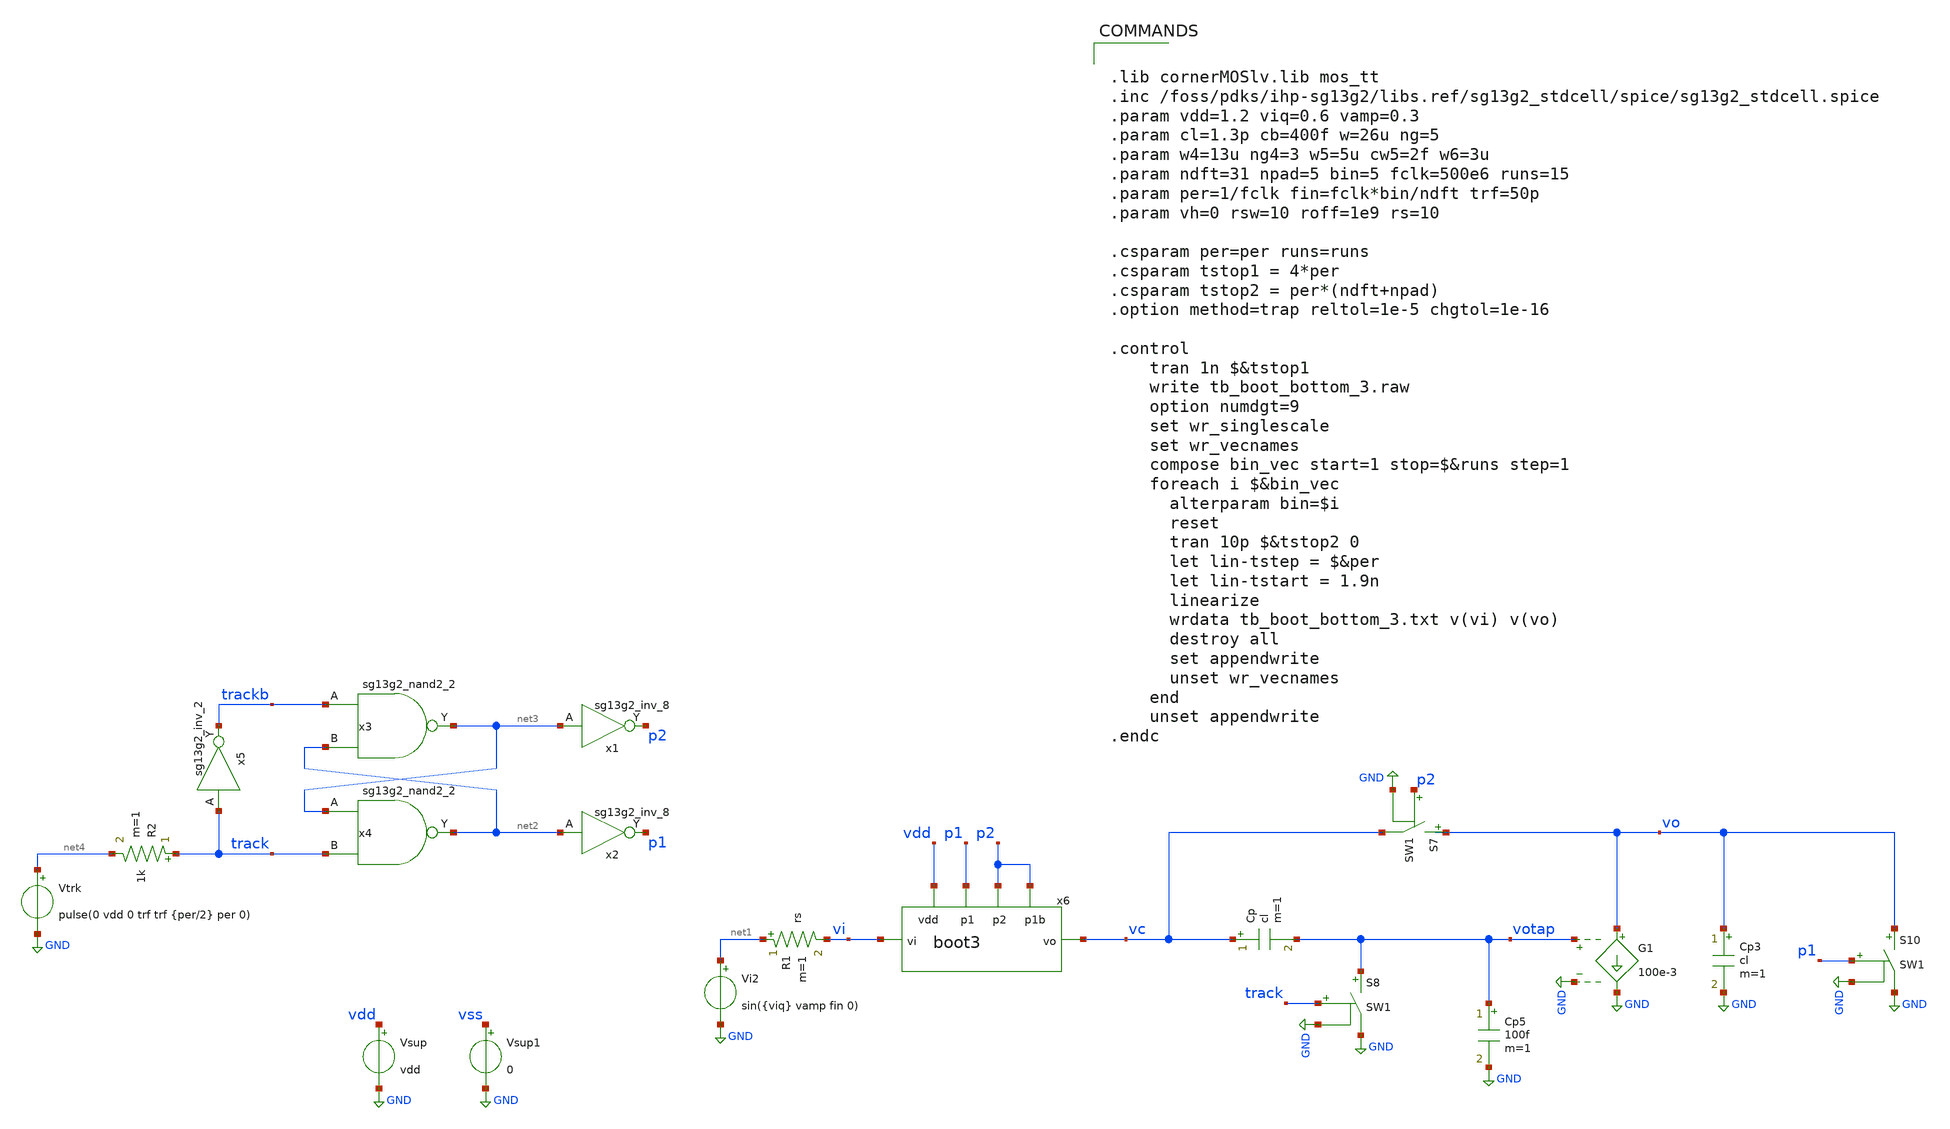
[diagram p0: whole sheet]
** sch_path: xschem/tb_boot_bottom_3.sch
* IHP-GmbH/IHP-Open-PDK/ihp-sg13g2/libs.tech/xschem/sg13g2_stdcells/sg13g2_inv_2.sch:
* Copyright 2023 IHP PDK Authors
* Licensed under the Apache License, Version 2.0 (the "License");
**.subckt tb_boot_bottom_3
Vi2 net1 GND sin({viq} vamp fin 0)
x1 p2 net3 VDD VSS sg13g2_inv_8
x2 p1 net2 VDD VSS sg13g2_inv_8
x3 net3 trackb net2 VDD VSS sg13g2_nand2_2
x4 net2 net3 track VDD VSS sg13g2_nand2_2
x5 trackb track VDD VSS sg13g2_inv_2
Vtrk net4 GND pulse(0 vdd 0 trf trf {per/2} per 0)
Vsup vdd GND vdd
Vsup1 vss GND 0
R1 net1 vi rs m=1
Cp vc votap cl m=1
G1 vo GND votap GND 100e-3
S7 vo vc p2 GND SW1
Cp3 vo GND cl m=1
S8 votap GND track GND SW1
S10 vo GND p1 GND SW1
Cp5 votap GND 100f m=1
x6 vdd p1 p2 vc vi p2 boot3
R2 track net4 1k m=1
**** begin user architecture code


.lib cornerMOSlv.lib mos_tt
.inc /foss/pdks/ihp-sg13g2/libs.ref/sg13g2_stdcell/spice/sg13g2_stdcell.spice
.param vdd=1.2 viq=0.6 vamp=0.3
.param cl=1.3p cb=400f w=26u ng=5
.param w4=13u ng4=3 w5=5u cw5=2f w6=3u
.param ndft=31 npad=5 bin=5 fclk=500e6 runs=15
.param per=1/fclk fin=fclk*bin/ndft trf=50p
.param vh=0 rsw=10 roff=1e9 rs=10

.csparam per=per runs=runs
.csparam tstop1 = 4*per
.csparam tstop2 = per*(ndft+npad)
.option method=trap reltol=1e-5 chgtol=1e-16

.control
    tran 1n $&tstop1
    write tb_boot_bottom_3.raw
    option numdgt=9
    set wr_singlescale
    set wr_vecnames
    compose bin_vec start=1 stop=$&runs step=1
    foreach i $&bin_vec
      alterparam bin=$i
      reset
      tran 10p $&tstop2 0
      let lin-tstep = $&per
      let lin-tstart = 1.9n
      linearize
      wrdata tb_boot_bottom_3.txt v(vi) v(vo)
      destroy all
      set appendwrite
      unset wr_vecnames
    end
    unset appendwrite
.endc


**** end user architecture code
**.ends

* expanding   symbol:  sg13g2_stdcells/sg13g2_inv_8.sym # of pins=2
** sym_path: sg13g2_stdcells/sg13g2_inv_8.sym
** sch_path: sg13g2_stdcells/sg13g2_inv_8.sch
.subckt sg13g2_inv_8 Y A VDD VSS
*.opin Y
*.ipin A
*.iopin VDD
*.iopin VSS
XM1 Y A VSS VSS sg13_lv_nmos w=5.92u l=130.00n ng=8 m=1 mm_ok=1
XM2 Y A VDD VDD sg13_lv_pmos w=8.96u l=130.00n ng=8 m=1 mm_ok=1
.ends


* expanding   symbol:  sg13g2_stdcells/sg13g2_nand2_2.sym # of pins=3
** sym_path: sg13g2_stdcells/sg13g2_nand2_2.sym
** sch_path: sg13g2_stdcells/sg13g2_nand2_2.sch
.subckt sg13g2_nand2_2 Y A B VDD VSS
*.iopin VDD
*.iopin VSS
*.opin Y
*.ipin B
*.ipin A
XM1 Y A net1 VSS sg13_lv_nmos w=1.44u l=130.00n ng=2 m=1 mm_ok=1
XM2 net1 B VSS VSS sg13_lv_nmos w=1.44u l=130.00n ng=2 m=1 mm_ok=1
XM3 Y A VDD VDD sg13_lv_pmos w=2.24u l=130.00n ng=2 m=1 mm_ok=1
XM4 Y B VDD VDD sg13_lv_pmos w=2.24u l=130.00n ng=2 m=1 mm_ok=1
.ends


* expanding   symbol:  sg13g2_stdcells/sg13g2_inv_2.sym # of pins=2
** sym_path: sg13g2_stdcells/sg13g2_inv_2.sym
** sch_path: sg13g2_stdcells/sg13g2_inv_2.sch
.subckt sg13g2_inv_2 Y A VDD VSS
*.opin Y
*.ipin A
*.iopin VDD
*.iopin VSS
XM1 Y A VSS VSS sg13_lv_nmos w=1.48u l=130.00n ng=2 m=1 mm_ok=1
XM2 Y A VDD VDD sg13_lv_pmos w=2.24u l=130.00n ng=2 m=1 mm_ok=1
.ends


* expanding   symbol:  boot3.sym # of pins=6
** sym_path: xschem/boot3.sym
** sch_path: xschem/boot3.sch
.subckt boot3 vdd p1 p2 vo vi p1b
*.ipin vi
*.opin vo
*.ipin p2
*.iopin vdd
*.ipin p1
*.ipin p1b
Cm1 vtop vbot cb m=1
S4 vi vbot p1 GND SW1
XM1 vi vg vo GND sg13_lv_nmos w=w l=0.13u ng=ng m=1 mm_ok=1
XM8 vg vdd net1 GND sg13_lv_nmos w=w4 l=0.13u ng=ng4 m=1 mm_ok=1
XM4 net1 p1b GND GND sg13_lv_nmos w=w4 l=0.13u ng=ng4 m=1 mm_ok=1
XM6 vbot p2 GND GND sg13_lv_nmos w=w6 l=0.13u ng=1 m=1 mm_ok=1
XM5 vtop vg vdd vtop sg13_lv_pmos w=w5 l=0.13u ng=1 m=1 mm_ok=1
S3 vg vtop p1 GND SW1
Cw5 vtop GND cw5 m=1
.ends

.GLOBAL GND
**** begin user architecture code
.MODEL SW1 SW   VT=0.6 VH=vh  RON=rsw ROFF=roff
**** end user architecture code
.end
